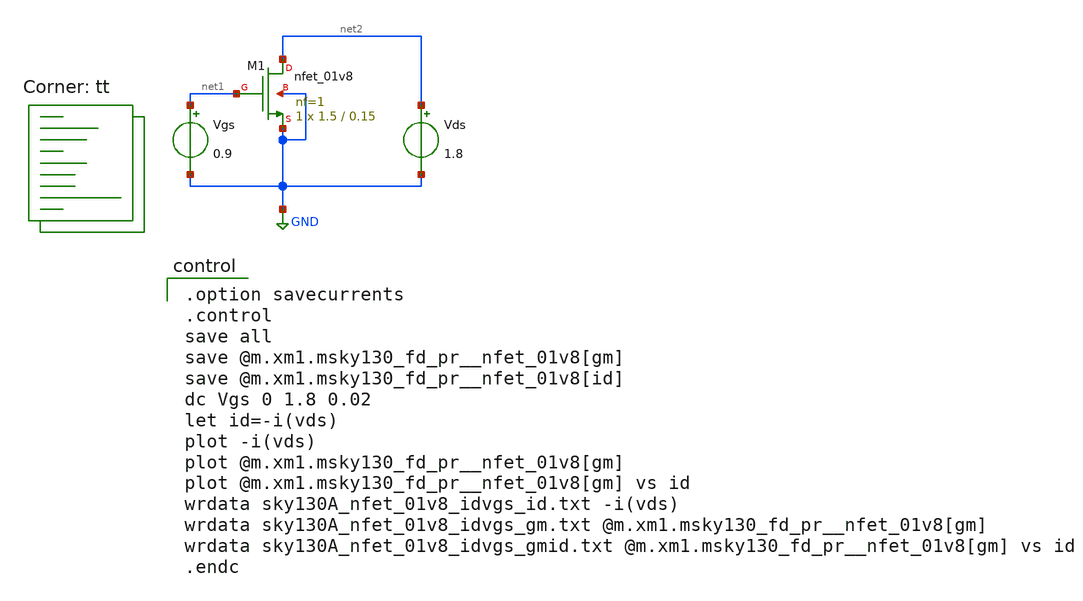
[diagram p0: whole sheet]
** sch_path: xschem/MOSFET/sky130A_nfet_01v8_idvgs.sch
**.subckt sky130A_nfet_01v8_idvgs
Vgs net1 GND 0.9
Vds net2 GND 1.8
XM1 net2 net1 GND GND sky130_fd_pr__nfet_01v8 L=0.15 W=1.5 nf=1 ad='int((1 + 1)/2) * 1.5 / 1 * 0.29'
+ as='int((1 + 2)/2) * 1.5 / 1 * 0.29' pd='2*int((1 + 1)/2) * (1.5 / 1 + 0.29)' ps='2*int((1 + 2)/2) * (1.5 / 1 + 0.29)'
+ nrd='0.29 / 1.5 ' nrs='0.29 / 1.5 ' sa=0 sb=0 sd=0 mult=1 m=1
**** begin user architecture code

.option savecurrents
.control
save all
save @m.xm1.msky130_fd_pr__nfet_01v8[gm]
save @m.xm1.msky130_fd_pr__nfet_01v8[id]
dc Vgs 0 1.8 0.02
let id=-i(vds)
plot -i(vds)
plot @m.xm1.msky130_fd_pr__nfet_01v8[gm]
plot @m.xm1.msky130_fd_pr__nfet_01v8[gm] vs id
wrdata sky130A_nfet_01v8_idvgs_id.txt -i(vds)
wrdata sky130A_nfet_01v8_idvgs_gm.txt @m.xm1.msky130_fd_pr__nfet_01v8[gm]
wrdata sky130A_nfet_01v8_idvgs_gmid.txt @m.xm1.msky130_fd_pr__nfet_01v8[gm] vs id
.endc

.lib $::SKYWATER_MODELS/sky130.lib.spice tt
**** end user architecture code
**.ends
.GLOBAL GND
.end
